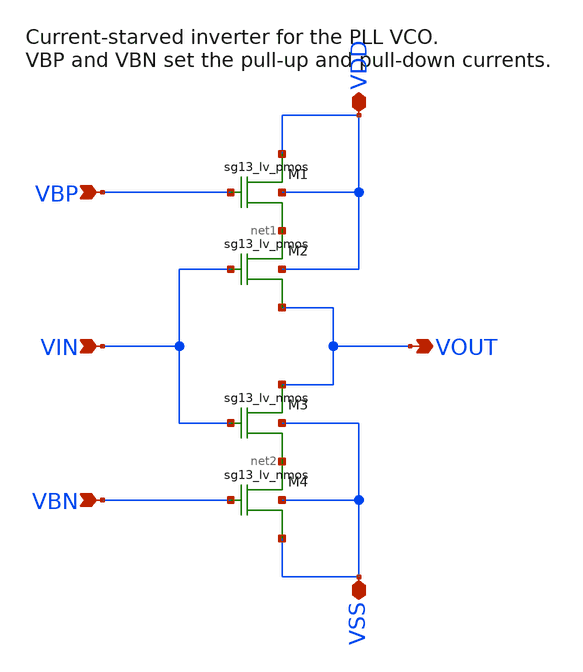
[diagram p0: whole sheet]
** sch_path: macros/pll_analog/schematic/xschem/inverter.sch
**.subckt inverter VIN VBP VBN VOUT VDD VSS
*.ipin VIN
*.ipin VBP
*.ipin VBN
*.opin VOUT
*.iopin VDD
*.iopin VSS
XM1 VDD VBP net1 VDD sg13_lv_pmos w=4.5u l=0.13u ng=5 m=1
XM2 net1 VIN VOUT VDD sg13_lv_pmos w=0.9u l=0.13u ng=1 m=1
XM3 VOUT VIN net2 VSS sg13_lv_nmos w=0.9u l=0.13u ng=1 m=1
XM4 net2 VBN VSS VSS sg13_lv_nmos w=4.5u l=0.13u ng=5 m=1
**.ends
.end
